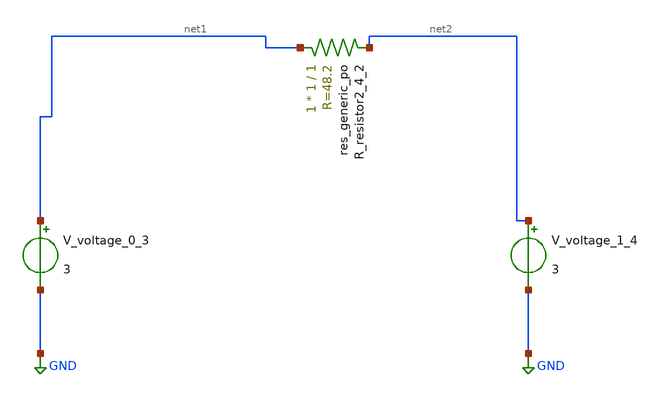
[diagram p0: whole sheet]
** sch_path: schematics/AMSNet/792.sch
**.subckt 792
XR_resistor2_4_2 net1 net2 sky130_fd_pr__res_generic_po W=1 L=1 m=1
V_voltage_0_3 net1 GND 3
V_voltage_1_4 net2 GND 3
**.ends
.GLOBAL GND
.end
